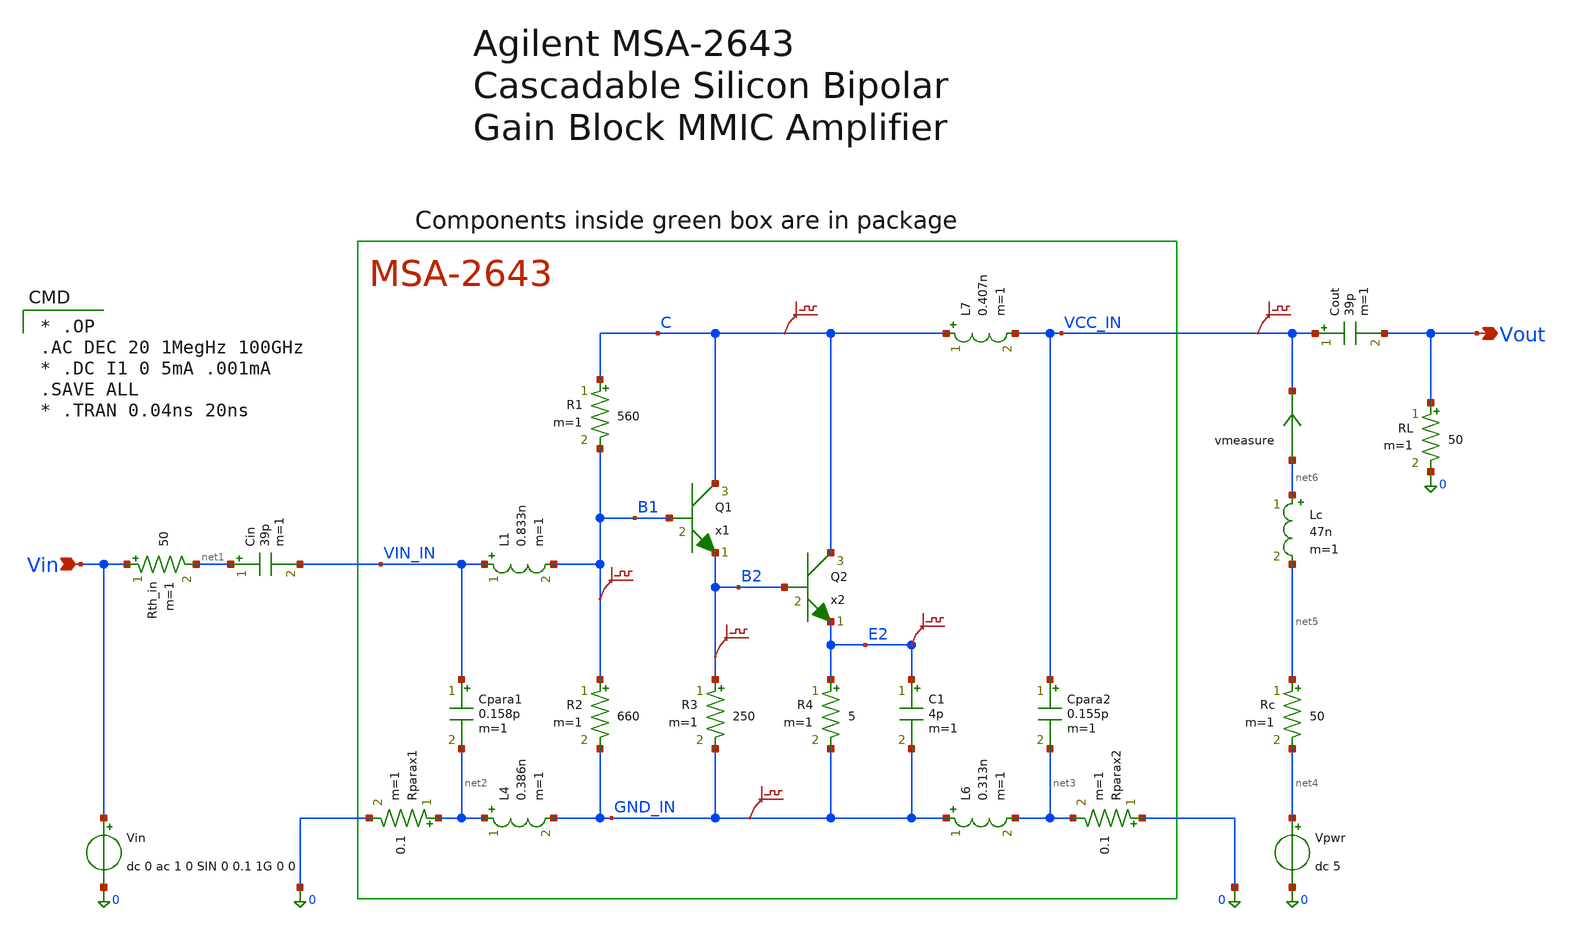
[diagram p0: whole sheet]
** sch_path: xschem_library/examples/MSA-2643.sch
* Copyright (C) 1998-2024 Stefan Frederik Schippers
* This program is free software; you can redistribute it and/or modify
* it under the terms of the GNU General Public License as published by
* the Free Software Foundation; either version 2 of the License, or
* (at your option) any later version.
* This program is distributed in the hope that it will be useful,
* but WITHOUT ANY WARRANTY; without even the implied warranty of
* MERCHANTABILITY or FITNESS FOR A PARTICULAR PURPOSE.  See the
* GNU General Public License for more details.
* You should have received a copy of the GNU General Public License
* along with this program; if not, write to the Free Software
* xschem_library/examples/Q2.sym:
* Copyright (C) 1998-2023 Stefan Frederik Schippers
**.subckt MSA-2643 Vout Vin
*.opin Vout
*.ipin Vin
x1 C B1 B2 Q1
x2 C B2 E2 Q2
Vin Vin 0 dc 0 ac 1 0 SIN 0 0.1 1G 0 0
Rth_in Vin net1 50 m=1
Cin net1 VIN_IN 39p m=1
L1 VIN_IN B1 0.833n m=1
Cpara1 VIN_IN net2 0.158p m=1
L4 net2 GND_IN 0.386n m=1
R1 C B1 560 m=1
R2 B1 GND_IN 660 m=1
R3 B2 GND_IN 250 m=1
R4 E2 GND_IN 5 m=1
C1 E2 GND_IN 4p m=1
L6 GND_IN net3 0.313n m=1
Cpara2 VCC_IN net3 0.155p m=1
L7 C VCC_IN 0.407n m=1
Vpwr net4 0 dc 5
Rc net5 net4 50 m=1
Lc net6 net5 47n m=1
Cout VCC_IN Vout 39p m=1
RL Vout 0 50 m=1
Rparax1 net2 0 0.1 m=1
Rparax2 0 net3 0.1 m=1
vmeasure net6 VCC_IN 0
.save i(vmeasure)
.save v(vcc_in)
.save v(c)
.save v(b1)
.save v(b2)
.save v(e2)
.save v(gnd_in)
**** begin user architecture code

* .OP
.AC DEC 20 1MegHz 100GHz
* .DC I1 0 5mA .001mA
.SAVE ALL
* .TRAN 0.04ns 20ns


**** end user architecture code
**.ends

* expanding   symbol:  Q1.sym # of pins=3
** sym_path: xschem_library/examples/Q1.sym
** sch_path: xschem_library/examples/Q1.sch
.subckt Q1 P3 P2 P1
*.iopin P3
*.iopin P1
*.iopin P2
**** begin user architecture code

* This is the BJT model used in the Agilent MSA-26 model
* documented in 5980-2496E.pdf.
* Model entered 3.31.2003 by SDB
.model BJTM1_Q1   NPN(Bf=1e6 IKF=5.895e-1 ISE=2.838e-19 NE=1.006   VAF=44 NF=1 TF=5.37e-12 XTF=20
+ VTF=0.8 ITF=2.218e-1 PTF=22   XTB=0.7 BR=1 IKR=1.1e-2 NC=2 VAR=3.37 NR=1.005 TR=4e-9   EG=1.17 IS=4.475e-18
+ XTI=3 TNOM=21 CJC=2.921e-14   VJC=0.6775 MJC=0.3319 XCJC=4.398e-1 FC=0.8 CJE=7.546e-14    VJE=0.9907
+ MJE=0.5063 RB=9.301 IRB=8.18e-5 RBM=0.1 KF=1.643e-23)

* This is a diode model used in the Agilent MSA-26 model
* documented in 5980-2496E.pdf.
* Model entered 3.31.2003 by SDB
.model DIODEM1_Q1   D(IS=1.405e-17 N=1 CJO=2.281e-14    VJ=0.729 M=0.44 FC=0.8 TNOM=21)

* This is a diode model used in the Agilent MSA-26 model
* documented in 5980-2496E.pdf.
* Model entered 3.31.2003 by SDB
.model DIODEM2_Q1   D(IS=1e-24 N=1.0029 CJO=2.452e-14    VJ=0.8971 M=0.2292 FC=0.8 TNOM=21)




**** end user architecture code
Rcx P3 C 6.386 TC1=0.113e-2 m=1
Re E P1 2.158 m=1
Rbx P2 B 3.723 TC1=0.14e-2 m=1
Q1 C B E BJTM1_Q1 area=1 m=1
D1 P2 C DiodeM1_Q1 area=1
Ccox P2 C 1.851e-14 m=1
Ceox B P1 6.01e-15 m=1
D2 B E DiodeM2_Q1 area=1
.ends


* expanding   symbol:  Q2.sym # of pins=3
** sym_path: xschem_library/examples/Q2.sym
** sch_path: xschem_library/examples/Q2.sch
.subckt Q2 P3 P2 P1
*.iopin P3
*.iopin P1
*.iopin P2
**** begin user architecture code

* This is the BJT model used in the Agilent MSA-26 model
* documented in 5980-2496E.pdf.
* Model entered 3.30.2003 by SDB
.model BJTM1_Q2   NPN(Bf=1e6 IKF=5.895e-1 ISE=2.838e-19 NE=1.006   VAF=44 NF=1 TF=5.37e-12 XTF=20
+ VTF=0.8 ITF=8.872e-1 PTF=22   XTB=0.7 BR=1 IKR=4.4e-2 NC=2 VAR=3.37 NR=1.005 TR=4e-9   EG=1.17 IS=1.79e-17
+ XTI=3 TNOM=21 CJC=3.717e-14   VJC=0.6775 MJC=0.3319 XCJC=4.398e-1 FC=0.8 CJE=3.217e-13    VJE=0.9907
+ MJE=0.5063 RB=2.325 IRB=3.272e-4 RBM=2.5e-2 KF=1.026e-24)

* This is a diode model used in the Agilent MSA-26 model
* documented in 5980-2496E.pdf.
* Model entered 3.30.2003 by SDB
.model DIODEM1_Q2   D(IS=5.62e-17 N=1 CJO=9.676e-14    VJ=0.729 M=0.44 FC=0.8 TNOM=21)

* This is a diode model used in the Agilent MSA-26 model
* documented in 5980-2496E.pdf.
* Model entered 3.30.2003 by SDB
.model DIODEM2_Q2   D(IS=1e-24 N=1.0029 CJO=9.023e-14    VJ=0.8971 M=2.292e-1 FC=0.8 TNOM=21)



**** end user architecture code
Rcx P3 C 1.716 TC1=0.113e-2 m=1
Re E P1 0.443 m=1
Rbx P2 B 0.463 TC1=0.14e-2 m=1
Q1 C B E BJTM1_Q2 area=4 m=1
D1 P2 C DiodeM1_Q2 area=1
Ccox P2 C 6.598e-14 m=1
Ceox B P1 2.417e-14 m=1
D2 B E DiodeM2_Q2 area=1
.ends

.end
